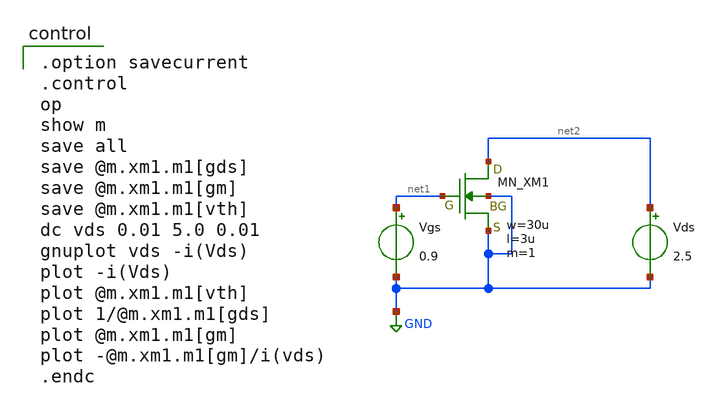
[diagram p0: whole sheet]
** sch_path: IO_202604/06/xschem/nfet_idvds.sch
**.subckt nfet_idvds
Vgs net1 GND 0.9
Vds net2 GND 2.5
XM1 net2 net1 GND GND NMOS w=30u l=3u as=0 ad=0 ps=0 pd=0 nrd=0 nrs=0 m=1
**** begin user architecture code

.option savecurrent
.control
op
show m
save all
save @m.xm1.m1[gds]
save @m.xm1.m1[gm]
save @m.xm1.m1[vth]
dc vds 0.01 5.0 0.01
gnuplot vds -i(Vds)
plot -i(Vds)
plot @m.xm1.m1[vth]
plot 1/@m.xm1.m1[gds]
plot @m.xm1.m1[gm]
plot -@m.xm1.m1[gm]/i(vds)
.endc

 .include $::LIB/../ip62_models
**** end user architecture code
**.ends
.GLOBAL GND
.end
